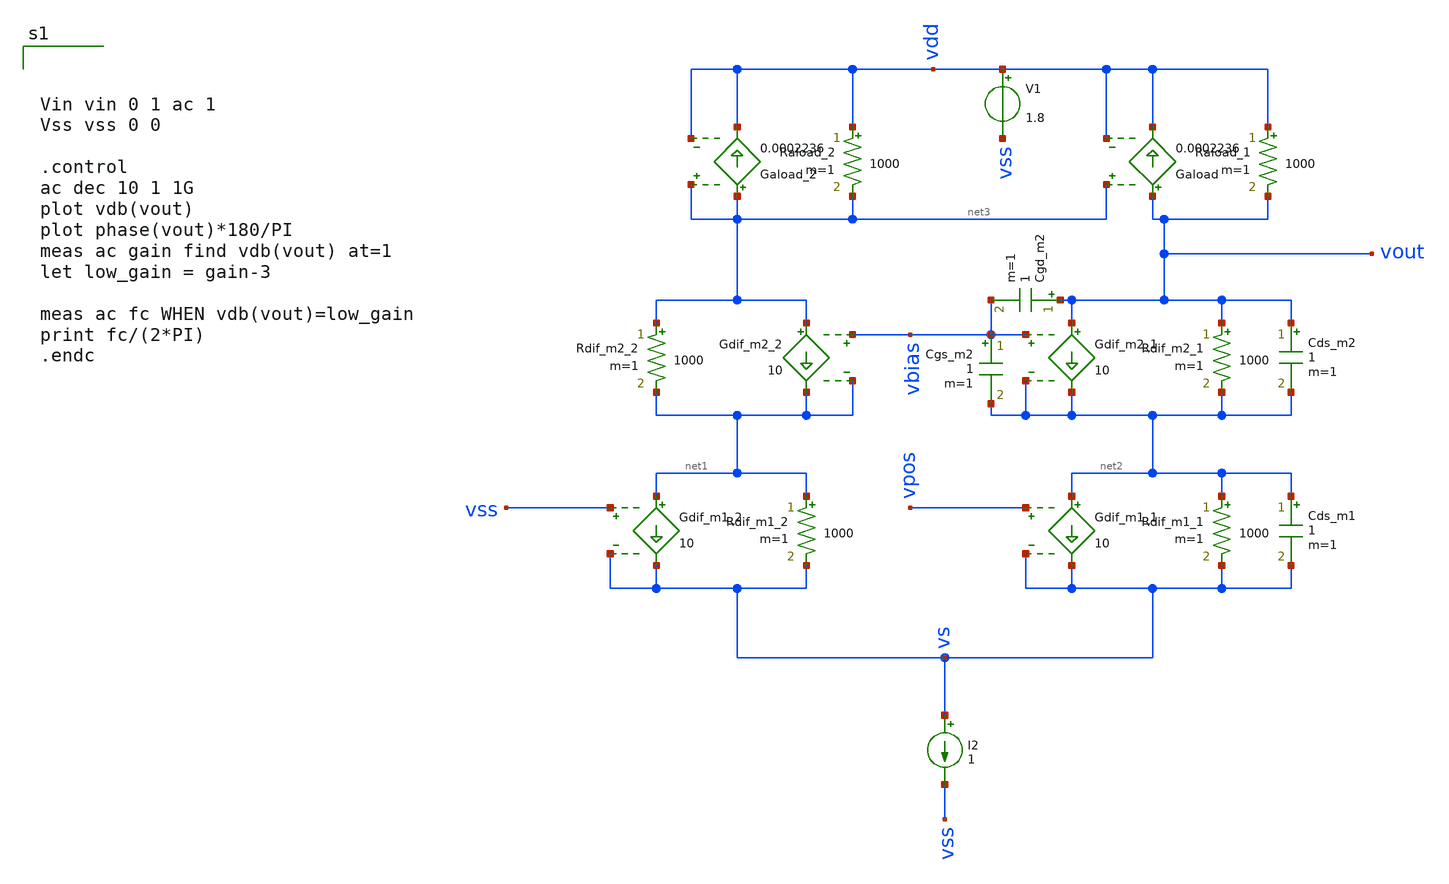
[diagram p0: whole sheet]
** sch_path: test-python/sstadex/untitled-3.sch
**.subckt untitled-3
Rdif_m1_2 net1 vs 1000 m=1
Gdif_m1_2 net1 vs vss vs 10
Rdif_m1_1 net2 vs 1000 m=1
Gdif_m1_1 net2 vs vpos vs 10
I2 vs vss 1
V1 vdd vss 1.8
Raload_1 vdd vout 1000 m=1
Raload_2 vdd net3 1000 m=1
Gaload vout vdd net3 vdd 0.0002236
Gaload_2 net3 vdd net3 vdd 0.0002236
Rdif_m2_1 vout net2 1000 m=1
Gdif_m2_1 vout net2 vbias net2 10
Rdif_m2_2 net3 net1 1000 m=1
Gdif_m2_2 net3 net1 vbias net1 10
Cds_m1 net2 vs 1 m=1
Cds_m2 vout net2 1 m=1
Cgs_m2 vbias net2 1 m=1
Cgd_m2 vout vbias 1 m=1
**** begin user architecture code



Vin vin 0 1 ac 1
Vss vss 0 0

.control
ac dec 10 1 1G
plot vdb(vout)
plot phase(vout)*180/PI
meas ac gain find vdb(vout) at=1
let low_gain = gain-3

meas ac fc WHEN vdb(vout)=low_gain
print fc/(2*PI)
.endc



**** end user architecture code
**.ends
.end
